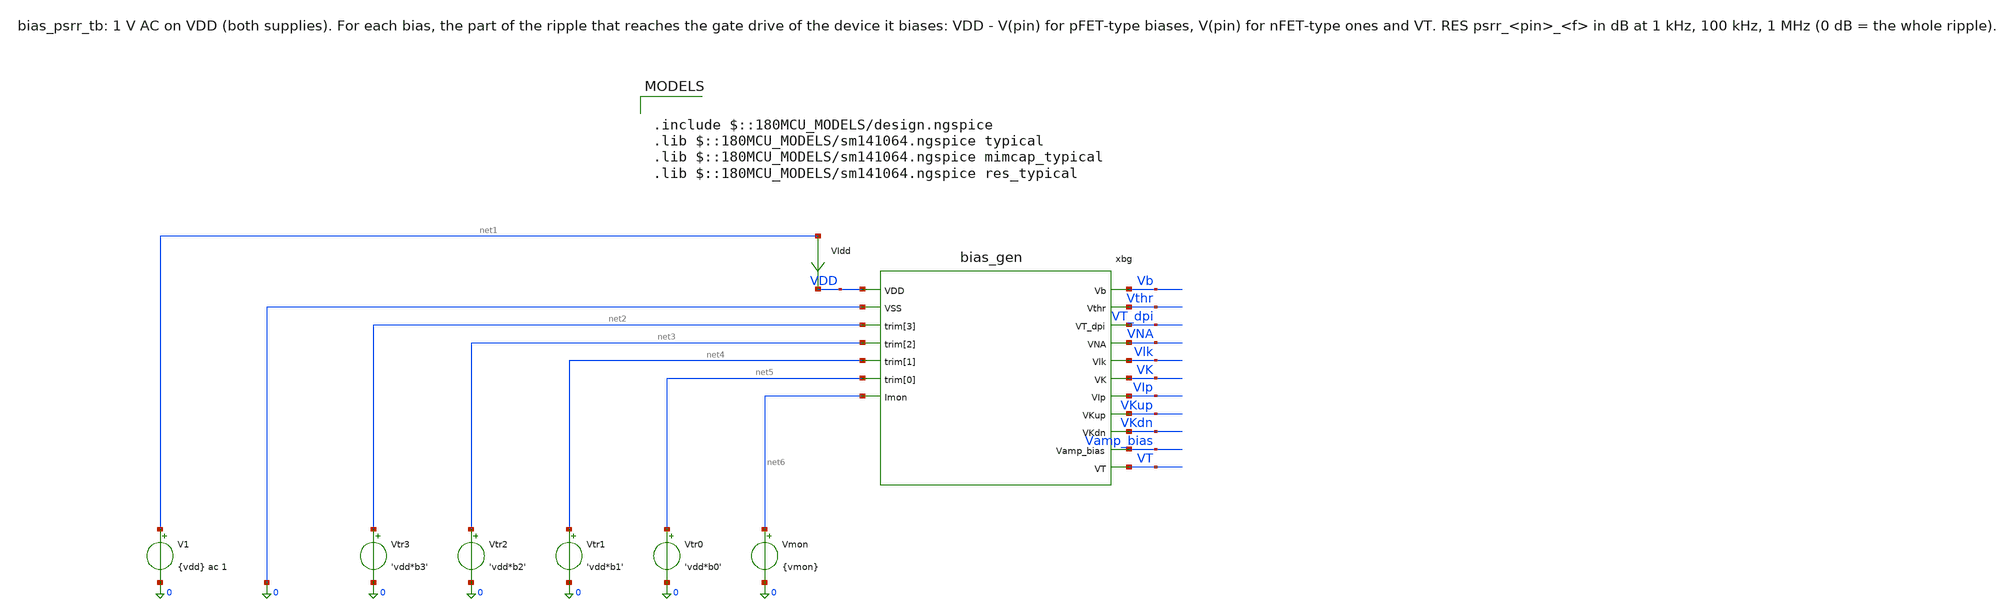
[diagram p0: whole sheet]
** sch_path: analog/bias/testbenches/bias_psrr_tb.sch
**.subckt bias_psrr_tb
xbg VDD 0 net2 net3 net4 net5 net6 Vb Vthr VT_dpi VNA Vlk VK VIp VKup VKdn Vamp_bias VT bias_gen
V1 net1 0 {vdd} ac 1
VIdd net1 VDD 0
.save i(vidd)
Vtr3 net2 0 'vdd*b3'
Vtr2 net3 0 'vdd*b2'
Vtr1 net4 0 'vdd*b1'
Vtr0 net5 0 'vdd*b0'
Vmon net6 0 {vmon}
**** begin user architecture code

.include $::180MCU_MODELS/design.ngspice
.lib $::180MCU_MODELS/sm141064.ngspice typical
.lib $::180MCU_MODELS/sm141064.ngspice mimcap_typical
.lib $::180MCU_MODELS/sm141064.ngspice res_typical



.param vdd=3.3 code=9 vmon=1.65
* trim bits of 'code' (b3 = MSB), driven by Vtr3..Vtr0
.param b3='floor(code/8)-2*floor(code/16)' b2='floor(code/4)-2*floor(code/8)'
.param b1='floor(code/2)-2*floor(code/4)' b0='code-2*floor(code/2)'
.csparam code_c={code}
.csparam vdd_c={vdd}
.control
  save all
  ac dec 10 1 100meg
  let ps_Vb = db(v(Vb))
  meas ac psrr_Vb_1k find ps_Vb at=1k
  echo RES psrr_Vb_1k=$&psrr_Vb_1k
  meas ac psrr_Vb_100k find ps_Vb at=100k
  echo RES psrr_Vb_100k=$&psrr_Vb_100k
  meas ac psrr_Vb_1M find ps_Vb at=1meg
  echo RES psrr_Vb_1M=$&psrr_Vb_1M
  let ps_Vthr = db(1 - v(Vthr))
  meas ac psrr_Vthr_1k find ps_Vthr at=1k
  echo RES psrr_Vthr_1k=$&psrr_Vthr_1k
  meas ac psrr_Vthr_100k find ps_Vthr at=100k
  echo RES psrr_Vthr_100k=$&psrr_Vthr_100k
  meas ac psrr_Vthr_1M find ps_Vthr at=1meg
  echo RES psrr_Vthr_1M=$&psrr_Vthr_1M
  let ps_VT_dpi = db(1 - v(VT_dpi))
  meas ac psrr_VT_dpi_1k find ps_VT_dpi at=1k
  echo RES psrr_VT_dpi_1k=$&psrr_VT_dpi_1k
  meas ac psrr_VT_dpi_100k find ps_VT_dpi at=100k
  echo RES psrr_VT_dpi_100k=$&psrr_VT_dpi_100k
  meas ac psrr_VT_dpi_1M find ps_VT_dpi at=1meg
  echo RES psrr_VT_dpi_1M=$&psrr_VT_dpi_1M
  let ps_VNA = db(1 - v(VNA))
  meas ac psrr_VNA_1k find ps_VNA at=1k
  echo RES psrr_VNA_1k=$&psrr_VNA_1k
  meas ac psrr_VNA_100k find ps_VNA at=100k
  echo RES psrr_VNA_100k=$&psrr_VNA_100k
  meas ac psrr_VNA_1M find ps_VNA at=1meg
  echo RES psrr_VNA_1M=$&psrr_VNA_1M
  let ps_Vlk = db(v(Vlk))
  meas ac psrr_Vlk_1k find ps_Vlk at=1k
  echo RES psrr_Vlk_1k=$&psrr_Vlk_1k
  meas ac psrr_Vlk_100k find ps_Vlk at=100k
  echo RES psrr_Vlk_100k=$&psrr_Vlk_100k
  meas ac psrr_Vlk_1M find ps_Vlk at=1meg
  echo RES psrr_Vlk_1M=$&psrr_Vlk_1M
  let ps_VK = db(v(VK))
  meas ac psrr_VK_1k find ps_VK at=1k
  echo RES psrr_VK_1k=$&psrr_VK_1k
  meas ac psrr_VK_100k find ps_VK at=100k
  echo RES psrr_VK_100k=$&psrr_VK_100k
  meas ac psrr_VK_1M find ps_VK at=1meg
  echo RES psrr_VK_1M=$&psrr_VK_1M
  let ps_VIp = db(v(VIp))
  meas ac psrr_VIp_1k find ps_VIp at=1k
  echo RES psrr_VIp_1k=$&psrr_VIp_1k
  meas ac psrr_VIp_100k find ps_VIp at=100k
  echo RES psrr_VIp_100k=$&psrr_VIp_100k
  meas ac psrr_VIp_1M find ps_VIp at=1meg
  echo RES psrr_VIp_1M=$&psrr_VIp_1M
  let ps_VKup = db(1 - v(VKup))
  meas ac psrr_VKup_1k find ps_VKup at=1k
  echo RES psrr_VKup_1k=$&psrr_VKup_1k
  meas ac psrr_VKup_100k find ps_VKup at=100k
  echo RES psrr_VKup_100k=$&psrr_VKup_100k
  meas ac psrr_VKup_1M find ps_VKup at=1meg
  echo RES psrr_VKup_1M=$&psrr_VKup_1M
  let ps_VKdn = db(v(VKdn))
  meas ac psrr_VKdn_1k find ps_VKdn at=1k
  echo RES psrr_VKdn_1k=$&psrr_VKdn_1k
  meas ac psrr_VKdn_100k find ps_VKdn at=100k
  echo RES psrr_VKdn_100k=$&psrr_VKdn_100k
  meas ac psrr_VKdn_1M find ps_VKdn at=1meg
  echo RES psrr_VKdn_1M=$&psrr_VKdn_1M
  let ps_Vamp_bias = db(v(Vamp_bias))
  meas ac psrr_Vamp_bias_1k find ps_Vamp_bias at=1k
  echo RES psrr_Vamp_bias_1k=$&psrr_Vamp_bias_1k
  meas ac psrr_Vamp_bias_100k find ps_Vamp_bias at=100k
  echo RES psrr_Vamp_bias_100k=$&psrr_Vamp_bias_100k
  meas ac psrr_Vamp_bias_1M find ps_Vamp_bias at=1meg
  echo RES psrr_Vamp_bias_1M=$&psrr_Vamp_bias_1M
  let ps_VT = db(v(VT))
  meas ac psrr_VT_1k find ps_VT at=1k
  echo RES psrr_VT_1k=$&psrr_VT_1k
  meas ac psrr_VT_100k find ps_VT at=100k
  echo RES psrr_VT_100k=$&psrr_VT_100k
  meas ac psrr_VT_1M find ps_VT at=1meg
  echo RES psrr_VT_1M=$&psrr_VT_1M
  if $?batchmode = 0
    plot ps_Vthr ps_VT_dpi ps_Vlk ps_VK ps_VNA ps_VT xlog title 'Supply ripple at the gate drive (dB)'
  end
.endc


**** end user architecture code
**.ends

* expanding   symbol:  analog/bias/bias_gen.sym # of pins=18
** sym_path: analog/bias/bias_gen.sym
** sch_path: analog/bias/bias_gen.sch
.subckt bias_gen VDD VSS trim[3] trim[2] trim[1] trim[0] Imon Vb Vthr VT_dpi VNA Vlk VK VIp VKup
+ VKdn Vamp_bias VT
*.iopin VDD
*.iopin VSS
*.ipin trim[3]
*.ipin trim[2]
*.ipin trim[1]
*.ipin trim[0]
*.iopin Imon
*.opin Vb
*.opin Vthr
*.opin VT_dpi
*.opin VNA
*.opin Vlk
*.opin VK
*.opin VIp
*.opin VKup
*.opin VKdn
*.opin Vamp_bias
*.opin VT
XM3 Vgp Vgp VDD VDD pfet_03v3 L=6.0u W=1.0u nf=1 ad='int((nf+1)/2) * W/nf * 0.18u' as='int((nf+2)/2) * W/nf * 0.18u'
+ pd='2*int((nf+1)/2) * (W/nf + 0.18u)' ps='2*int((nf+2)/2) * (W/nf + 0.18u)' nrd='0.18u / W' nrs='0.18u / W'
+ sa=0 sb=0 sd=0 m=4
XM4 Vgn Vgp VDD VDD pfet_03v3 L=6.0u W=1.0u nf=1 ad='int((nf+1)/2) * W/nf * 0.18u' as='int((nf+2)/2) * W/nf * 0.18u'
+ pd='2*int((nf+1)/2) * (W/nf + 0.18u)' ps='2*int((nf+2)/2) * (W/nf + 0.18u)' nrd='0.18u / W' nrs='0.18u / W'
+ sa=0 sb=0 sd=0 m=4
XM2 Vgp Vgn Vr VSS nfet_03v3 L=6.0u W=1.0u nf=1 ad='int((nf+1)/2) * W/nf * 0.18u' as='int((nf+2)/2) * W/nf * 0.18u'
+ pd='2*int((nf+1)/2) * (W/nf + 0.18u)' ps='2*int((nf+2)/2) * (W/nf + 0.18u)' nrd='0.18u / W' nrs='0.18u / W'
+ sa=0 sb=0 sd=0 m=64
XM1 Vgn Vgn VSS VSS nfet_03v3 L=6.0u W=1.0u nf=1 ad='int((nf+1)/2) * W/nf * 0.18u' as='int((nf+2)/2) * W/nf * 0.18u'
+ pd='2*int((nf+1)/2) * (W/nf + 0.18u)' ps='2*int((nf+2)/2) * (W/nf + 0.18u)' nrd='0.18u / W' nrs='0.18u / W'
+ sa=0 sb=0 sd=0 m=8
XR15 t3 Vr VSS nwell r_width=2.0e-6 r_length=367.830e-6 m=1
XRT3 t2 t3 VSS nwell r_width=2.0e-6 r_length=178.750e-6 m=1
XMT3 t3 trim[3] t2 VSS nfet_03v3 L=0.28u W=4.0u nf=1 ad='int((nf+1)/2) * W/nf * 0.18u' as='int((nf+2)/2) * W/nf * 0.18u'
+ pd='2*int((nf+1)/2) * (W/nf + 0.18u)' ps='2*int((nf+2)/2) * (W/nf + 0.18u)' nrd='0.18u / W' nrs='0.18u / W'
+ sa=0 sb=0 sd=0 m=4
XRT2 t1 t2 VSS nwell r_width=2.0e-6 r_length=89.375e-6 m=1
XMT2 t2 trim[2] t1 VSS nfet_03v3 L=0.28u W=4.0u nf=1 ad='int((nf+1)/2) * W/nf * 0.18u' as='int((nf+2)/2) * W/nf * 0.18u'
+ pd='2*int((nf+1)/2) * (W/nf + 0.18u)' ps='2*int((nf+2)/2) * (W/nf + 0.18u)' nrd='0.18u / W' nrs='0.18u / W'
+ sa=0 sb=0 sd=0 m=2
XRT1 t0 t1 VSS nwell r_width=2.0e-6 r_length=44.687e-6 m=1
XMT1 t1 trim[1] t0 VSS nfet_03v3 L=0.28u W=4.0u nf=1 ad='int((nf+1)/2) * W/nf * 0.18u' as='int((nf+2)/2) * W/nf * 0.18u'
+ pd='2*int((nf+1)/2) * (W/nf + 0.18u)' ps='2*int((nf+2)/2) * (W/nf + 0.18u)' nrd='0.18u / W' nrs='0.18u / W'
+ sa=0 sb=0 sd=0 m=1
XRT0 VSS t0 VSS nwell r_width=2.0e-6 r_length=22.344e-6 m=1
XMT0 t0 trim[0] VSS VSS nfet_03v3 L=0.28u W=4.0u nf=1 ad='int((nf+1)/2) * W/nf * 0.18u' as='int((nf+2)/2) * W/nf * 0.18u'
+ pd='2*int((nf+1)/2) * (W/nf + 0.18u)' ps='2*int((nf+2)/2) * (W/nf + 0.18u)' nrd='0.18u / W' nrs='0.18u / W'
+ sa=0 sb=0 sd=0 m=1
XMS1_0 net1 VSS VDD VDD pfet_03v3 L=50u W=0.22u nf=1 ad='int((nf+1)/2) * W/nf * 0.18u' as='int((nf+2)/2) * W/nf * 0.18u'
+ pd='2*int((nf+1)/2) * (W/nf + 0.18u)' ps='2*int((nf+2)/2) * (W/nf + 0.18u)' nrd='0.18u / W' nrs='0.18u / W'
+ sa=0 sb=0 sd=0 m=1
XMS1_1 net2 VSS net1 VDD pfet_03v3 L=50u W=0.22u nf=1 ad='int((nf+1)/2) * W/nf * 0.18u' as='int((nf+2)/2) * W/nf * 0.18u'
+ pd='2*int((nf+1)/2) * (W/nf + 0.18u)' ps='2*int((nf+2)/2) * (W/nf + 0.18u)' nrd='0.18u / W' nrs='0.18u / W'
+ sa=0 sb=0 sd=0 m=1
XMS1_2 net3 VSS net2 VDD pfet_03v3 L=50u W=0.22u nf=1 ad='int((nf+1)/2) * W/nf * 0.18u' as='int((nf+2)/2) * W/nf * 0.18u'
+ pd='2*int((nf+1)/2) * (W/nf + 0.18u)' ps='2*int((nf+2)/2) * (W/nf + 0.18u)' nrd='0.18u / W' nrs='0.18u / W'
+ sa=0 sb=0 sd=0 m=1
XMS1_3 X VSS net3 VDD pfet_03v3 L=50u W=0.22u nf=1 ad='int((nf+1)/2) * W/nf * 0.18u' as='int((nf+2)/2) * W/nf * 0.18u'
+ pd='2*int((nf+1)/2) * (W/nf + 0.18u)' ps='2*int((nf+2)/2) * (W/nf + 0.18u)' nrd='0.18u / W' nrs='0.18u / W'
+ sa=0 sb=0 sd=0 m=1
XMS2 X Vgn VSS VSS nfet_03v3 L=6.0u W=1.0u nf=1 ad='int((nf+1)/2) * W/nf * 0.18u' as='int((nf+2)/2) * W/nf * 0.18u'
+ pd='2*int((nf+1)/2) * (W/nf + 0.18u)' ps='2*int((nf+2)/2) * (W/nf + 0.18u)' nrd='0.18u / W' nrs='0.18u / W'
+ sa=0 sb=0 sd=0 m=16
XMS3 Vgp X VSS VSS nfet_03v3 L=4u W=0.5u nf=1 ad='int((nf+1)/2) * W/nf * 0.18u' as='int((nf+2)/2) * W/nf * 0.18u'
+ pd='2*int((nf+1)/2) * (W/nf + 0.18u)' ps='2*int((nf+2)/2) * (W/nf + 0.18u)' nrd='0.18u / W' nrs='0.18u / W'
+ sa=0 sb=0 sd=0 m=1
XMMON Imon Vgn VSS VSS nfet_03v3 L=6.0u W=1.0u nf=1 ad='int((nf+1)/2) * W/nf * 0.18u' as='int((nf+2)/2) * W/nf * 0.18u'
+ pd='2*int((nf+1)/2) * (W/nf + 0.18u)' ps='2*int((nf+2)/2) * (W/nf + 0.18u)' nrd='0.18u / W' nrs='0.18u / W'
+ sa=0 sb=0 sd=0 m=8
XMOVB_0 net4 Vgp VDD VDD pfet_03v3 L=6.0u W=1.0u nf=1 ad='int((nf+1)/2) * W/nf * 0.18u' as='int((nf+2)/2) * W/nf * 0.18u'
+ pd='2*int((nf+1)/2) * (W/nf + 0.18u)' ps='2*int((nf+2)/2) * (W/nf + 0.18u)' nrd='0.18u / W' nrs='0.18u / W'
+ sa=0 sb=0 sd=0 m=5
XMOVB_1 net5 Vgp net4 VDD pfet_03v3 L=6.0u W=1.0u nf=1 ad='int((nf+1)/2) * W/nf * 0.18u' as='int((nf+2)/2) * W/nf * 0.18u'
+ pd='2*int((nf+1)/2) * (W/nf + 0.18u)' ps='2*int((nf+2)/2) * (W/nf + 0.18u)' nrd='0.18u / W' nrs='0.18u / W'
+ sa=0 sb=0 sd=0 m=5
XMOVB_2 net6 Vgp net5 VDD pfet_03v3 L=6.0u W=1.0u nf=1 ad='int((nf+1)/2) * W/nf * 0.18u' as='int((nf+2)/2) * W/nf * 0.18u'
+ pd='2*int((nf+1)/2) * (W/nf + 0.18u)' ps='2*int((nf+2)/2) * (W/nf + 0.18u)' nrd='0.18u / W' nrs='0.18u / W'
+ sa=0 sb=0 sd=0 m=5
XMOVB_3 net7 Vgp net6 VDD pfet_03v3 L=6.0u W=1.0u nf=1 ad='int((nf+1)/2) * W/nf * 0.18u' as='int((nf+2)/2) * W/nf * 0.18u'
+ pd='2*int((nf+1)/2) * (W/nf + 0.18u)' ps='2*int((nf+2)/2) * (W/nf + 0.18u)' nrd='0.18u / W' nrs='0.18u / W'
+ sa=0 sb=0 sd=0 m=5
XMOVB_4 net8 Vgp net7 VDD pfet_03v3 L=6.0u W=1.0u nf=1 ad='int((nf+1)/2) * W/nf * 0.18u' as='int((nf+2)/2) * W/nf * 0.18u'
+ pd='2*int((nf+1)/2) * (W/nf + 0.18u)' ps='2*int((nf+2)/2) * (W/nf + 0.18u)' nrd='0.18u / W' nrs='0.18u / W'
+ sa=0 sb=0 sd=0 m=5
XMOVB_5 Vb Vgp net8 VDD pfet_03v3 L=6.0u W=1.0u nf=1 ad='int((nf+1)/2) * W/nf * 0.18u' as='int((nf+2)/2) * W/nf * 0.18u'
+ pd='2*int((nf+1)/2) * (W/nf + 0.18u)' ps='2*int((nf+2)/2) * (W/nf + 0.18u)' nrd='0.18u / W' nrs='0.18u / W'
+ sa=0 sb=0 sd=0 m=5
XMRVB Vb Vb VSS VSS nfet_03v3 L=8.0u W=1.0u nf=1 ad='int((nf+1)/2) * W/nf * 0.18u' as='int((nf+2)/2) * W/nf * 0.18u'
+ pd='2*int((nf+1)/2) * (W/nf + 0.18u)' ps='2*int((nf+2)/2) * (W/nf + 0.18u)' nrd='0.18u / W' nrs='0.18u / W'
+ sa=0 sb=0 sd=0 m=3
XMCVB VSS Vb VSS VSS nfet_03v3 L=10.0u W=10.0u nf=1 ad='int((nf+1)/2) * W/nf * 0.18u' as='int((nf+2)/2) * W/nf * 0.18u'
+ pd='2*int((nf+1)/2) * (W/nf + 0.18u)' ps='2*int((nf+2)/2) * (W/nf + 0.18u)' nrd='0.18u / W' nrs='0.18u / W'
+ sa=0 sb=0 sd=0 m=1
XMRVTHR Vthr Vthr VDD VDD pfet_03v3 L=0.28u W=0.22u nf=1 ad='int((nf+1)/2) * W/nf * 0.18u' as='int((nf+2)/2) * W/nf * 0.18u'
+ pd='2*int((nf+1)/2) * (W/nf + 0.18u)' ps='2*int((nf+2)/2) * (W/nf + 0.18u)' nrd='0.18u / W' nrs='0.18u / W'
+ sa=0 sb=0 sd=0 m=32
XMOVTHR_0 Vthr Vgn net9 VSS nfet_03v3 L=6.0u W=1.0u nf=1 ad='int((nf+1)/2) * W/nf * 0.18u' as='int((nf+2)/2) * W/nf * 0.18u'
+ pd='2*int((nf+1)/2) * (W/nf + 0.18u)' ps='2*int((nf+2)/2) * (W/nf + 0.18u)' nrd='0.18u / W' nrs='0.18u / W'
+ sa=0 sb=0 sd=0 m=1
XMOVTHR_1 net9 Vgn net10 VSS nfet_03v3 L=6.0u W=1.0u nf=1 ad='int((nf+1)/2) * W/nf * 0.18u' as='int((nf+2)/2) * W/nf * 0.18u'
+ pd='2*int((nf+1)/2) * (W/nf + 0.18u)' ps='2*int((nf+2)/2) * (W/nf + 0.18u)' nrd='0.18u / W' nrs='0.18u / W'
+ sa=0 sb=0 sd=0 m=1
XMOVTHR_2 net10 Vgn net11 VSS nfet_03v3 L=6.0u W=1.0u nf=1 ad='int((nf+1)/2) * W/nf * 0.18u' as='int((nf+2)/2) * W/nf * 0.18u'
+ pd='2*int((nf+1)/2) * (W/nf + 0.18u)' ps='2*int((nf+2)/2) * (W/nf + 0.18u)' nrd='0.18u / W' nrs='0.18u / W'
+ sa=0 sb=0 sd=0 m=1
XMOVTHR_3 net11 Vgn net12 VSS nfet_03v3 L=6.0u W=1.0u nf=1 ad='int((nf+1)/2) * W/nf * 0.18u' as='int((nf+2)/2) * W/nf * 0.18u'
+ pd='2*int((nf+1)/2) * (W/nf + 0.18u)' ps='2*int((nf+2)/2) * (W/nf + 0.18u)' nrd='0.18u / W' nrs='0.18u / W'
+ sa=0 sb=0 sd=0 m=1
XMOVTHR_4 net12 Vgn net13 VSS nfet_03v3 L=6.0u W=1.0u nf=1 ad='int((nf+1)/2) * W/nf * 0.18u' as='int((nf+2)/2) * W/nf * 0.18u'
+ pd='2*int((nf+1)/2) * (W/nf + 0.18u)' ps='2*int((nf+2)/2) * (W/nf + 0.18u)' nrd='0.18u / W' nrs='0.18u / W'
+ sa=0 sb=0 sd=0 m=1
XMOVTHR_5 net13 Vgn net14 VSS nfet_03v3 L=6.0u W=1.0u nf=1 ad='int((nf+1)/2) * W/nf * 0.18u' as='int((nf+2)/2) * W/nf * 0.18u'
+ pd='2*int((nf+1)/2) * (W/nf + 0.18u)' ps='2*int((nf+2)/2) * (W/nf + 0.18u)' nrd='0.18u / W' nrs='0.18u / W'
+ sa=0 sb=0 sd=0 m=1
XMOVTHR_6 net14 Vgn net15 VSS nfet_03v3 L=6.0u W=1.0u nf=1 ad='int((nf+1)/2) * W/nf * 0.18u' as='int((nf+2)/2) * W/nf * 0.18u'
+ pd='2*int((nf+1)/2) * (W/nf + 0.18u)' ps='2*int((nf+2)/2) * (W/nf + 0.18u)' nrd='0.18u / W' nrs='0.18u / W'
+ sa=0 sb=0 sd=0 m=1
XMOVTHR_7 net15 Vgn net16 VSS nfet_03v3 L=6.0u W=1.0u nf=1 ad='int((nf+1)/2) * W/nf * 0.18u' as='int((nf+2)/2) * W/nf * 0.18u'
+ pd='2*int((nf+1)/2) * (W/nf + 0.18u)' ps='2*int((nf+2)/2) * (W/nf + 0.18u)' nrd='0.18u / W' nrs='0.18u / W'
+ sa=0 sb=0 sd=0 m=1
XMOVTHR_8 net16 Vgn net17 VSS nfet_03v3 L=6.0u W=1.0u nf=1 ad='int((nf+1)/2) * W/nf * 0.18u' as='int((nf+2)/2) * W/nf * 0.18u'
+ pd='2*int((nf+1)/2) * (W/nf + 0.18u)' ps='2*int((nf+2)/2) * (W/nf + 0.18u)' nrd='0.18u / W' nrs='0.18u / W'
+ sa=0 sb=0 sd=0 m=1
XMOVTHR_9 net17 Vgn net18 VSS nfet_03v3 L=6.0u W=1.0u nf=1 ad='int((nf+1)/2) * W/nf * 0.18u' as='int((nf+2)/2) * W/nf * 0.18u'
+ pd='2*int((nf+1)/2) * (W/nf + 0.18u)' ps='2*int((nf+2)/2) * (W/nf + 0.18u)' nrd='0.18u / W' nrs='0.18u / W'
+ sa=0 sb=0 sd=0 m=1
XMOVTHR_10 net18 Vgn net19 VSS nfet_03v3 L=6.0u W=1.0u nf=1 ad='int((nf+1)/2) * W/nf * 0.18u' as='int((nf+2)/2) * W/nf * 0.18u'
+ pd='2*int((nf+1)/2) * (W/nf + 0.18u)' ps='2*int((nf+2)/2) * (W/nf + 0.18u)' nrd='0.18u / W' nrs='0.18u / W'
+ sa=0 sb=0 sd=0 m=1
XMOVTHR_11 net19 Vgn net20 VSS nfet_03v3 L=6.0u W=1.0u nf=1 ad='int((nf+1)/2) * W/nf * 0.18u' as='int((nf+2)/2) * W/nf * 0.18u'
+ pd='2*int((nf+1)/2) * (W/nf + 0.18u)' ps='2*int((nf+2)/2) * (W/nf + 0.18u)' nrd='0.18u / W' nrs='0.18u / W'
+ sa=0 sb=0 sd=0 m=1
XMOVTHR_12 net20 Vgn net21 VSS nfet_03v3 L=6.0u W=1.0u nf=1 ad='int((nf+1)/2) * W/nf * 0.18u' as='int((nf+2)/2) * W/nf * 0.18u'
+ pd='2*int((nf+1)/2) * (W/nf + 0.18u)' ps='2*int((nf+2)/2) * (W/nf + 0.18u)' nrd='0.18u / W' nrs='0.18u / W'
+ sa=0 sb=0 sd=0 m=1
XMOVTHR_13 net21 Vgn net22 VSS nfet_03v3 L=6.0u W=1.0u nf=1 ad='int((nf+1)/2) * W/nf * 0.18u' as='int((nf+2)/2) * W/nf * 0.18u'
+ pd='2*int((nf+1)/2) * (W/nf + 0.18u)' ps='2*int((nf+2)/2) * (W/nf + 0.18u)' nrd='0.18u / W' nrs='0.18u / W'
+ sa=0 sb=0 sd=0 m=1
XMOVTHR_14 net22 Vgn VSS VSS nfet_03v3 L=6.0u W=1.0u nf=1 ad='int((nf+1)/2) * W/nf * 0.18u' as='int((nf+2)/2) * W/nf * 0.18u'
+ pd='2*int((nf+1)/2) * (W/nf + 0.18u)' ps='2*int((nf+2)/2) * (W/nf + 0.18u)' nrd='0.18u / W' nrs='0.18u / W'
+ sa=0 sb=0 sd=0 m=1
XMCVTHR VDD Vthr VDD VDD pfet_03v3 L=10.0u W=10.0u nf=1 ad='int((nf+1)/2) * W/nf * 0.18u' as='int((nf+2)/2) * W/nf * 0.18u'
+ pd='2*int((nf+1)/2) * (W/nf + 0.18u)' ps='2*int((nf+2)/2) * (W/nf + 0.18u)' nrd='0.18u / W' nrs='0.18u / W'
+ sa=0 sb=0 sd=0 m=1
XMRVT_DPI VT_dpi VT_dpi VDD VDD pfet_03v3 L=0.28u W=0.22u nf=1 ad='int((nf+1)/2) * W/nf * 0.18u' as='int((nf+2)/2) * W/nf * 0.18u'
+ pd='2*int((nf+1)/2) * (W/nf + 0.18u)' ps='2*int((nf+2)/2) * (W/nf + 0.18u)' nrd='0.18u / W' nrs='0.18u / W'
+ sa=0 sb=0 sd=0 m=32
XMOVT_DPI_0 VT_dpi Vgn net23 VSS nfet_03v3 L=6.0u W=1.0u nf=1 ad='int((nf+1)/2) * W/nf * 0.18u' as='int((nf+2)/2) * W/nf * 0.18u'
+ pd='2*int((nf+1)/2) * (W/nf + 0.18u)' ps='2*int((nf+2)/2) * (W/nf + 0.18u)' nrd='0.18u / W' nrs='0.18u / W'
+ sa=0 sb=0 sd=0 m=2
XMOVT_DPI_1 net23 Vgn net24 VSS nfet_03v3 L=6.0u W=1.0u nf=1 ad='int((nf+1)/2) * W/nf * 0.18u' as='int((nf+2)/2) * W/nf * 0.18u'
+ pd='2*int((nf+1)/2) * (W/nf + 0.18u)' ps='2*int((nf+2)/2) * (W/nf + 0.18u)' nrd='0.18u / W' nrs='0.18u / W'
+ sa=0 sb=0 sd=0 m=2
XMOVT_DPI_2 net24 Vgn net25 VSS nfet_03v3 L=6.0u W=1.0u nf=1 ad='int((nf+1)/2) * W/nf * 0.18u' as='int((nf+2)/2) * W/nf * 0.18u'
+ pd='2*int((nf+1)/2) * (W/nf + 0.18u)' ps='2*int((nf+2)/2) * (W/nf + 0.18u)' nrd='0.18u / W' nrs='0.18u / W'
+ sa=0 sb=0 sd=0 m=2
XMOVT_DPI_3 net25 Vgn net26 VSS nfet_03v3 L=6.0u W=1.0u nf=1 ad='int((nf+1)/2) * W/nf * 0.18u' as='int((nf+2)/2) * W/nf * 0.18u'
+ pd='2*int((nf+1)/2) * (W/nf + 0.18u)' ps='2*int((nf+2)/2) * (W/nf + 0.18u)' nrd='0.18u / W' nrs='0.18u / W'
+ sa=0 sb=0 sd=0 m=2
XMOVT_DPI_4 net26 Vgn net27 VSS nfet_03v3 L=6.0u W=1.0u nf=1 ad='int((nf+1)/2) * W/nf * 0.18u' as='int((nf+2)/2) * W/nf * 0.18u'
+ pd='2*int((nf+1)/2) * (W/nf + 0.18u)' ps='2*int((nf+2)/2) * (W/nf + 0.18u)' nrd='0.18u / W' nrs='0.18u / W'
+ sa=0 sb=0 sd=0 m=2
XMOVT_DPI_5 net27 Vgn net28 VSS nfet_03v3 L=6.0u W=1.0u nf=1 ad='int((nf+1)/2) * W/nf * 0.18u' as='int((nf+2)/2) * W/nf * 0.18u'
+ pd='2*int((nf+1)/2) * (W/nf + 0.18u)' ps='2*int((nf+2)/2) * (W/nf + 0.18u)' nrd='0.18u / W' nrs='0.18u / W'
+ sa=0 sb=0 sd=0 m=2
XMOVT_DPI_6 net28 Vgn net29 VSS nfet_03v3 L=6.0u W=1.0u nf=1 ad='int((nf+1)/2) * W/nf * 0.18u' as='int((nf+2)/2) * W/nf * 0.18u'
+ pd='2*int((nf+1)/2) * (W/nf + 0.18u)' ps='2*int((nf+2)/2) * (W/nf + 0.18u)' nrd='0.18u / W' nrs='0.18u / W'
+ sa=0 sb=0 sd=0 m=2
XMOVT_DPI_7 net29 Vgn net30 VSS nfet_03v3 L=6.0u W=1.0u nf=1 ad='int((nf+1)/2) * W/nf * 0.18u' as='int((nf+2)/2) * W/nf * 0.18u'
+ pd='2*int((nf+1)/2) * (W/nf + 0.18u)' ps='2*int((nf+2)/2) * (W/nf + 0.18u)' nrd='0.18u / W' nrs='0.18u / W'
+ sa=0 sb=0 sd=0 m=2
XMOVT_DPI_8 net30 Vgn net31 VSS nfet_03v3 L=6.0u W=1.0u nf=1 ad='int((nf+1)/2) * W/nf * 0.18u' as='int((nf+2)/2) * W/nf * 0.18u'
+ pd='2*int((nf+1)/2) * (W/nf + 0.18u)' ps='2*int((nf+2)/2) * (W/nf + 0.18u)' nrd='0.18u / W' nrs='0.18u / W'
+ sa=0 sb=0 sd=0 m=2
XMOVT_DPI_9 net31 Vgn net32 VSS nfet_03v3 L=6.0u W=1.0u nf=1 ad='int((nf+1)/2) * W/nf * 0.18u' as='int((nf+2)/2) * W/nf * 0.18u'
+ pd='2*int((nf+1)/2) * (W/nf + 0.18u)' ps='2*int((nf+2)/2) * (W/nf + 0.18u)' nrd='0.18u / W' nrs='0.18u / W'
+ sa=0 sb=0 sd=0 m=2
XMOVT_DPI_10 net32 Vgn net33 VSS nfet_03v3 L=6.0u W=1.0u nf=1 ad='int((nf+1)/2) * W/nf * 0.18u' as='int((nf+2)/2) * W/nf * 0.18u'
+ pd='2*int((nf+1)/2) * (W/nf + 0.18u)' ps='2*int((nf+2)/2) * (W/nf + 0.18u)' nrd='0.18u / W' nrs='0.18u / W'
+ sa=0 sb=0 sd=0 m=2
XMOVT_DPI_11 net33 Vgn net34 VSS nfet_03v3 L=6.0u W=1.0u nf=1 ad='int((nf+1)/2) * W/nf * 0.18u' as='int((nf+2)/2) * W/nf * 0.18u'
+ pd='2*int((nf+1)/2) * (W/nf + 0.18u)' ps='2*int((nf+2)/2) * (W/nf + 0.18u)' nrd='0.18u / W' nrs='0.18u / W'
+ sa=0 sb=0 sd=0 m=2
XMOVT_DPI_12 net34 Vgn net35 VSS nfet_03v3 L=6.0u W=1.0u nf=1 ad='int((nf+1)/2) * W/nf * 0.18u' as='int((nf+2)/2) * W/nf * 0.18u'
+ pd='2*int((nf+1)/2) * (W/nf + 0.18u)' ps='2*int((nf+2)/2) * (W/nf + 0.18u)' nrd='0.18u / W' nrs='0.18u / W'
+ sa=0 sb=0 sd=0 m=2
XMOVT_DPI_13 net35 Vgn net36 VSS nfet_03v3 L=6.0u W=1.0u nf=1 ad='int((nf+1)/2) * W/nf * 0.18u' as='int((nf+2)/2) * W/nf * 0.18u'
+ pd='2*int((nf+1)/2) * (W/nf + 0.18u)' ps='2*int((nf+2)/2) * (W/nf + 0.18u)' nrd='0.18u / W' nrs='0.18u / W'
+ sa=0 sb=0 sd=0 m=2
XMOVT_DPI_14 net36 Vgn net37 VSS nfet_03v3 L=6.0u W=1.0u nf=1 ad='int((nf+1)/2) * W/nf * 0.18u' as='int((nf+2)/2) * W/nf * 0.18u'
+ pd='2*int((nf+1)/2) * (W/nf + 0.18u)' ps='2*int((nf+2)/2) * (W/nf + 0.18u)' nrd='0.18u / W' nrs='0.18u / W'
+ sa=0 sb=0 sd=0 m=2
XMOVT_DPI_15 net37 Vgn net38 VSS nfet_03v3 L=6.0u W=1.0u nf=1 ad='int((nf+1)/2) * W/nf * 0.18u' as='int((nf+2)/2) * W/nf * 0.18u'
+ pd='2*int((nf+1)/2) * (W/nf + 0.18u)' ps='2*int((nf+2)/2) * (W/nf + 0.18u)' nrd='0.18u / W' nrs='0.18u / W'
+ sa=0 sb=0 sd=0 m=2
XMOVT_DPI_16 net38 Vgn net39 VSS nfet_03v3 L=6.0u W=1.0u nf=1 ad='int((nf+1)/2) * W/nf * 0.18u' as='int((nf+2)/2) * W/nf * 0.18u'
+ pd='2*int((nf+1)/2) * (W/nf + 0.18u)' ps='2*int((nf+2)/2) * (W/nf + 0.18u)' nrd='0.18u / W' nrs='0.18u / W'
+ sa=0 sb=0 sd=0 m=2
XMOVT_DPI_17 net39 Vgn net40 VSS nfet_03v3 L=6.0u W=1.0u nf=1 ad='int((nf+1)/2) * W/nf * 0.18u' as='int((nf+2)/2) * W/nf * 0.18u'
+ pd='2*int((nf+1)/2) * (W/nf + 0.18u)' ps='2*int((nf+2)/2) * (W/nf + 0.18u)' nrd='0.18u / W' nrs='0.18u / W'
+ sa=0 sb=0 sd=0 m=2
XMOVT_DPI_18 net40 Vgn net41 VSS nfet_03v3 L=6.0u W=1.0u nf=1 ad='int((nf+1)/2) * W/nf * 0.18u' as='int((nf+2)/2) * W/nf * 0.18u'
+ pd='2*int((nf+1)/2) * (W/nf + 0.18u)' ps='2*int((nf+2)/2) * (W/nf + 0.18u)' nrd='0.18u / W' nrs='0.18u / W'
+ sa=0 sb=0 sd=0 m=2
XMOVT_DPI_19 net41 Vgn net42 VSS nfet_03v3 L=6.0u W=1.0u nf=1 ad='int((nf+1)/2) * W/nf * 0.18u' as='int((nf+2)/2) * W/nf * 0.18u'
+ pd='2*int((nf+1)/2) * (W/nf + 0.18u)' ps='2*int((nf+2)/2) * (W/nf + 0.18u)' nrd='0.18u / W' nrs='0.18u / W'
+ sa=0 sb=0 sd=0 m=2
XMOVT_DPI_20 net42 Vgn net43 VSS nfet_03v3 L=6.0u W=1.0u nf=1 ad='int((nf+1)/2) * W/nf * 0.18u' as='int((nf+2)/2) * W/nf * 0.18u'
+ pd='2*int((nf+1)/2) * (W/nf + 0.18u)' ps='2*int((nf+2)/2) * (W/nf + 0.18u)' nrd='0.18u / W' nrs='0.18u / W'
+ sa=0 sb=0 sd=0 m=2
XMOVT_DPI_21 net43 Vgn net44 VSS nfet_03v3 L=6.0u W=1.0u nf=1 ad='int((nf+1)/2) * W/nf * 0.18u' as='int((nf+2)/2) * W/nf * 0.18u'
+ pd='2*int((nf+1)/2) * (W/nf + 0.18u)' ps='2*int((nf+2)/2) * (W/nf + 0.18u)' nrd='0.18u / W' nrs='0.18u / W'
+ sa=0 sb=0 sd=0 m=2
XMOVT_DPI_22 net44 Vgn VSS VSS nfet_03v3 L=6.0u W=1.0u nf=1 ad='int((nf+1)/2) * W/nf * 0.18u' as='int((nf+2)/2) * W/nf * 0.18u'
+ pd='2*int((nf+1)/2) * (W/nf + 0.18u)' ps='2*int((nf+2)/2) * (W/nf + 0.18u)' nrd='0.18u / W' nrs='0.18u / W'
+ sa=0 sb=0 sd=0 m=2
XMCVT_DPI VDD VT_dpi VDD VDD pfet_03v3 L=10.0u W=10.0u nf=1 ad='int((nf+1)/2) * W/nf * 0.18u' as='int((nf+2)/2) * W/nf * 0.18u'
+ pd='2*int((nf+1)/2) * (W/nf + 0.18u)' ps='2*int((nf+2)/2) * (W/nf + 0.18u)' nrd='0.18u / W' nrs='0.18u / W'
+ sa=0 sb=0 sd=0 m=1
XMRVNA_0 net45 VNA VDD VDD pfet_03v3 L=1.0u W=1.0u nf=1 ad='int((nf+1)/2) * W/nf * 0.18u' as='int((nf+2)/2) * W/nf * 0.18u'
+ pd='2*int((nf+1)/2) * (W/nf + 0.18u)' ps='2*int((nf+2)/2) * (W/nf + 0.18u)' nrd='0.18u / W' nrs='0.18u / W'
+ sa=0 sb=0 sd=0 m=1
XMRVNA_1 net46 VNA net45 VDD pfet_03v3 L=1.0u W=1.0u nf=1 ad='int((nf+1)/2) * W/nf * 0.18u' as='int((nf+2)/2) * W/nf * 0.18u'
+ pd='2*int((nf+1)/2) * (W/nf + 0.18u)' ps='2*int((nf+2)/2) * (W/nf + 0.18u)' nrd='0.18u / W' nrs='0.18u / W'
+ sa=0 sb=0 sd=0 m=1
XMRVNA_2 net47 VNA net46 VDD pfet_03v3 L=1.0u W=1.0u nf=1 ad='int((nf+1)/2) * W/nf * 0.18u' as='int((nf+2)/2) * W/nf * 0.18u'
+ pd='2*int((nf+1)/2) * (W/nf + 0.18u)' ps='2*int((nf+2)/2) * (W/nf + 0.18u)' nrd='0.18u / W' nrs='0.18u / W'
+ sa=0 sb=0 sd=0 m=1
XMRVNA_3 net48 VNA net47 VDD pfet_03v3 L=1.0u W=1.0u nf=1 ad='int((nf+1)/2) * W/nf * 0.18u' as='int((nf+2)/2) * W/nf * 0.18u'
+ pd='2*int((nf+1)/2) * (W/nf + 0.18u)' ps='2*int((nf+2)/2) * (W/nf + 0.18u)' nrd='0.18u / W' nrs='0.18u / W'
+ sa=0 sb=0 sd=0 m=1
XMRVNA_4 net49 VNA net48 VDD pfet_03v3 L=1.0u W=1.0u nf=1 ad='int((nf+1)/2) * W/nf * 0.18u' as='int((nf+2)/2) * W/nf * 0.18u'
+ pd='2*int((nf+1)/2) * (W/nf + 0.18u)' ps='2*int((nf+2)/2) * (W/nf + 0.18u)' nrd='0.18u / W' nrs='0.18u / W'
+ sa=0 sb=0 sd=0 m=1
XMRVNA_5 net50 VNA net49 VDD pfet_03v3 L=1.0u W=1.0u nf=1 ad='int((nf+1)/2) * W/nf * 0.18u' as='int((nf+2)/2) * W/nf * 0.18u'
+ pd='2*int((nf+1)/2) * (W/nf + 0.18u)' ps='2*int((nf+2)/2) * (W/nf + 0.18u)' nrd='0.18u / W' nrs='0.18u / W'
+ sa=0 sb=0 sd=0 m=1
XMRVNA_6 net51 VNA net50 VDD pfet_03v3 L=1.0u W=1.0u nf=1 ad='int((nf+1)/2) * W/nf * 0.18u' as='int((nf+2)/2) * W/nf * 0.18u'
+ pd='2*int((nf+1)/2) * (W/nf + 0.18u)' ps='2*int((nf+2)/2) * (W/nf + 0.18u)' nrd='0.18u / W' nrs='0.18u / W'
+ sa=0 sb=0 sd=0 m=1
XMRVNA_7 net52 VNA net51 VDD pfet_03v3 L=1.0u W=1.0u nf=1 ad='int((nf+1)/2) * W/nf * 0.18u' as='int((nf+2)/2) * W/nf * 0.18u'
+ pd='2*int((nf+1)/2) * (W/nf + 0.18u)' ps='2*int((nf+2)/2) * (W/nf + 0.18u)' nrd='0.18u / W' nrs='0.18u / W'
+ sa=0 sb=0 sd=0 m=1
XMRVNA_8 net53 VNA net52 VDD pfet_03v3 L=1.0u W=1.0u nf=1 ad='int((nf+1)/2) * W/nf * 0.18u' as='int((nf+2)/2) * W/nf * 0.18u'
+ pd='2*int((nf+1)/2) * (W/nf + 0.18u)' ps='2*int((nf+2)/2) * (W/nf + 0.18u)' nrd='0.18u / W' nrs='0.18u / W'
+ sa=0 sb=0 sd=0 m=1
XMRVNA_9 net54 VNA net53 VDD pfet_03v3 L=1.0u W=1.0u nf=1 ad='int((nf+1)/2) * W/nf * 0.18u' as='int((nf+2)/2) * W/nf * 0.18u'
+ pd='2*int((nf+1)/2) * (W/nf + 0.18u)' ps='2*int((nf+2)/2) * (W/nf + 0.18u)' nrd='0.18u / W' nrs='0.18u / W'
+ sa=0 sb=0 sd=0 m=1
XMRVNA_10 net55 VNA net54 VDD pfet_03v3 L=1.0u W=1.0u nf=1 ad='int((nf+1)/2) * W/nf * 0.18u' as='int((nf+2)/2) * W/nf * 0.18u'
+ pd='2*int((nf+1)/2) * (W/nf + 0.18u)' ps='2*int((nf+2)/2) * (W/nf + 0.18u)' nrd='0.18u / W' nrs='0.18u / W'
+ sa=0 sb=0 sd=0 m=1
XMRVNA_11 net56 VNA net55 VDD pfet_03v3 L=1.0u W=1.0u nf=1 ad='int((nf+1)/2) * W/nf * 0.18u' as='int((nf+2)/2) * W/nf * 0.18u'
+ pd='2*int((nf+1)/2) * (W/nf + 0.18u)' ps='2*int((nf+2)/2) * (W/nf + 0.18u)' nrd='0.18u / W' nrs='0.18u / W'
+ sa=0 sb=0 sd=0 m=1
XMRVNA_12 net57 VNA net56 VDD pfet_03v3 L=1.0u W=1.0u nf=1 ad='int((nf+1)/2) * W/nf * 0.18u' as='int((nf+2)/2) * W/nf * 0.18u'
+ pd='2*int((nf+1)/2) * (W/nf + 0.18u)' ps='2*int((nf+2)/2) * (W/nf + 0.18u)' nrd='0.18u / W' nrs='0.18u / W'
+ sa=0 sb=0 sd=0 m=1
XMRVNA_13 net58 VNA net57 VDD pfet_03v3 L=1.0u W=1.0u nf=1 ad='int((nf+1)/2) * W/nf * 0.18u' as='int((nf+2)/2) * W/nf * 0.18u'
+ pd='2*int((nf+1)/2) * (W/nf + 0.18u)' ps='2*int((nf+2)/2) * (W/nf + 0.18u)' nrd='0.18u / W' nrs='0.18u / W'
+ sa=0 sb=0 sd=0 m=1
XMRVNA_14 net59 VNA net58 VDD pfet_03v3 L=1.0u W=1.0u nf=1 ad='int((nf+1)/2) * W/nf * 0.18u' as='int((nf+2)/2) * W/nf * 0.18u'
+ pd='2*int((nf+1)/2) * (W/nf + 0.18u)' ps='2*int((nf+2)/2) * (W/nf + 0.18u)' nrd='0.18u / W' nrs='0.18u / W'
+ sa=0 sb=0 sd=0 m=1
XMRVNA_15 VNA VNA net59 VDD pfet_03v3 L=1.0u W=1.0u nf=1 ad='int((nf+1)/2) * W/nf * 0.18u' as='int((nf+2)/2) * W/nf * 0.18u'
+ pd='2*int((nf+1)/2) * (W/nf + 0.18u)' ps='2*int((nf+2)/2) * (W/nf + 0.18u)' nrd='0.18u / W' nrs='0.18u / W'
+ sa=0 sb=0 sd=0 m=1
XMOVNA_0 VNA Vgn net60 VSS nfet_03v3 L=6.0u W=1.0u nf=1 ad='int((nf+1)/2) * W/nf * 0.18u' as='int((nf+2)/2) * W/nf * 0.18u'
+ pd='2*int((nf+1)/2) * (W/nf + 0.18u)' ps='2*int((nf+2)/2) * (W/nf + 0.18u)' nrd='0.18u / W' nrs='0.18u / W'
+ sa=0 sb=0 sd=0 m=18
XMOVNA_1 net60 Vgn VSS VSS nfet_03v3 L=6.0u W=1.0u nf=1 ad='int((nf+1)/2) * W/nf * 0.18u' as='int((nf+2)/2) * W/nf * 0.18u'
+ pd='2*int((nf+1)/2) * (W/nf + 0.18u)' ps='2*int((nf+2)/2) * (W/nf + 0.18u)' nrd='0.18u / W' nrs='0.18u / W'
+ sa=0 sb=0 sd=0 m=18
XMCVNA VDD VNA VDD VDD pfet_03v3 L=10.0u W=10.0u nf=1 ad='int((nf+1)/2) * W/nf * 0.18u' as='int((nf+2)/2) * W/nf * 0.18u'
+ pd='2*int((nf+1)/2) * (W/nf + 0.18u)' ps='2*int((nf+2)/2) * (W/nf + 0.18u)' nrd='0.18u / W' nrs='0.18u / W'
+ sa=0 sb=0 sd=0 m=1
XMOVLK_0 net61 Vgp VDD VDD pfet_03v3 L=6.0u W=1.0u nf=1 ad='int((nf+1)/2) * W/nf * 0.18u' as='int((nf+2)/2) * W/nf * 0.18u'
+ pd='2*int((nf+1)/2) * (W/nf + 0.18u)' ps='2*int((nf+2)/2) * (W/nf + 0.18u)' nrd='0.18u / W' nrs='0.18u / W'
+ sa=0 sb=0 sd=0 m=1
XMOVLK_1 net62 Vgp net61 VDD pfet_03v3 L=6.0u W=1.0u nf=1 ad='int((nf+1)/2) * W/nf * 0.18u' as='int((nf+2)/2) * W/nf * 0.18u'
+ pd='2*int((nf+1)/2) * (W/nf + 0.18u)' ps='2*int((nf+2)/2) * (W/nf + 0.18u)' nrd='0.18u / W' nrs='0.18u / W'
+ sa=0 sb=0 sd=0 m=1
XMOVLK_2 net63 Vgp net62 VDD pfet_03v3 L=6.0u W=1.0u nf=1 ad='int((nf+1)/2) * W/nf * 0.18u' as='int((nf+2)/2) * W/nf * 0.18u'
+ pd='2*int((nf+1)/2) * (W/nf + 0.18u)' ps='2*int((nf+2)/2) * (W/nf + 0.18u)' nrd='0.18u / W' nrs='0.18u / W'
+ sa=0 sb=0 sd=0 m=1
XMOVLK_3 net64 Vgp net63 VDD pfet_03v3 L=6.0u W=1.0u nf=1 ad='int((nf+1)/2) * W/nf * 0.18u' as='int((nf+2)/2) * W/nf * 0.18u'
+ pd='2*int((nf+1)/2) * (W/nf + 0.18u)' ps='2*int((nf+2)/2) * (W/nf + 0.18u)' nrd='0.18u / W' nrs='0.18u / W'
+ sa=0 sb=0 sd=0 m=1
XMOVLK_4 net65 Vgp net64 VDD pfet_03v3 L=6.0u W=1.0u nf=1 ad='int((nf+1)/2) * W/nf * 0.18u' as='int((nf+2)/2) * W/nf * 0.18u'
+ pd='2*int((nf+1)/2) * (W/nf + 0.18u)' ps='2*int((nf+2)/2) * (W/nf + 0.18u)' nrd='0.18u / W' nrs='0.18u / W'
+ sa=0 sb=0 sd=0 m=1
XMOVLK_5 net66 Vgp net65 VDD pfet_03v3 L=6.0u W=1.0u nf=1 ad='int((nf+1)/2) * W/nf * 0.18u' as='int((nf+2)/2) * W/nf * 0.18u'
+ pd='2*int((nf+1)/2) * (W/nf + 0.18u)' ps='2*int((nf+2)/2) * (W/nf + 0.18u)' nrd='0.18u / W' nrs='0.18u / W'
+ sa=0 sb=0 sd=0 m=1
XMOVLK_6 Vlk Vgp net66 VDD pfet_03v3 L=6.0u W=1.0u nf=1 ad='int((nf+1)/2) * W/nf * 0.18u' as='int((nf+2)/2) * W/nf * 0.18u'
+ pd='2*int((nf+1)/2) * (W/nf + 0.18u)' ps='2*int((nf+2)/2) * (W/nf + 0.18u)' nrd='0.18u / W' nrs='0.18u / W'
+ sa=0 sb=0 sd=0 m=1
XMRVLK Vlk Vlk VSS VSS nfet_03v3 L=1.0u W=1.0u nf=1 ad='int((nf+1)/2) * W/nf * 0.18u' as='int((nf+2)/2) * W/nf * 0.18u'
+ pd='2*int((nf+1)/2) * (W/nf + 0.18u)' ps='2*int((nf+2)/2) * (W/nf + 0.18u)' nrd='0.18u / W' nrs='0.18u / W'
+ sa=0 sb=0 sd=0 m=14
XMCVLK VSS Vlk VSS VSS nfet_03v3 L=10.0u W=10.0u nf=1 ad='int((nf+1)/2) * W/nf * 0.18u' as='int((nf+2)/2) * W/nf * 0.18u'
+ pd='2*int((nf+1)/2) * (W/nf + 0.18u)' ps='2*int((nf+2)/2) * (W/nf + 0.18u)' nrd='0.18u / W' nrs='0.18u / W'
+ sa=0 sb=0 sd=0 m=1
XMOVK VK Vgp VDD VDD pfet_03v3 L=6.0u W=1.0u nf=1 ad='int((nf+1)/2) * W/nf * 0.18u' as='int((nf+2)/2) * W/nf * 0.18u'
+ pd='2*int((nf+1)/2) * (W/nf + 0.18u)' ps='2*int((nf+2)/2) * (W/nf + 0.18u)' nrd='0.18u / W' nrs='0.18u / W'
+ sa=0 sb=0 sd=0 m=17
XMRVK_0 VK VK net67 VSS nfet_03v3 L=1.0u W=1.0u nf=1 ad='int((nf+1)/2) * W/nf * 0.18u' as='int((nf+2)/2) * W/nf * 0.18u'
+ pd='2*int((nf+1)/2) * (W/nf + 0.18u)' ps='2*int((nf+2)/2) * (W/nf + 0.18u)' nrd='0.18u / W' nrs='0.18u / W'
+ sa=0 sb=0 sd=0 m=1
XMRVK_1 net67 VK net68 VSS nfet_03v3 L=1.0u W=1.0u nf=1 ad='int((nf+1)/2) * W/nf * 0.18u' as='int((nf+2)/2) * W/nf * 0.18u'
+ pd='2*int((nf+1)/2) * (W/nf + 0.18u)' ps='2*int((nf+2)/2) * (W/nf + 0.18u)' nrd='0.18u / W' nrs='0.18u / W'
+ sa=0 sb=0 sd=0 m=1
XMRVK_2 net68 VK net69 VSS nfet_03v3 L=1.0u W=1.0u nf=1 ad='int((nf+1)/2) * W/nf * 0.18u' as='int((nf+2)/2) * W/nf * 0.18u'
+ pd='2*int((nf+1)/2) * (W/nf + 0.18u)' ps='2*int((nf+2)/2) * (W/nf + 0.18u)' nrd='0.18u / W' nrs='0.18u / W'
+ sa=0 sb=0 sd=0 m=1
XMRVK_3 net69 VK net70 VSS nfet_03v3 L=1.0u W=1.0u nf=1 ad='int((nf+1)/2) * W/nf * 0.18u' as='int((nf+2)/2) * W/nf * 0.18u'
+ pd='2*int((nf+1)/2) * (W/nf + 0.18u)' ps='2*int((nf+2)/2) * (W/nf + 0.18u)' nrd='0.18u / W' nrs='0.18u / W'
+ sa=0 sb=0 sd=0 m=1
XMRVK_4 net70 VK net71 VSS nfet_03v3 L=1.0u W=1.0u nf=1 ad='int((nf+1)/2) * W/nf * 0.18u' as='int((nf+2)/2) * W/nf * 0.18u'
+ pd='2*int((nf+1)/2) * (W/nf + 0.18u)' ps='2*int((nf+2)/2) * (W/nf + 0.18u)' nrd='0.18u / W' nrs='0.18u / W'
+ sa=0 sb=0 sd=0 m=1
XMRVK_5 net71 VK net72 VSS nfet_03v3 L=1.0u W=1.0u nf=1 ad='int((nf+1)/2) * W/nf * 0.18u' as='int((nf+2)/2) * W/nf * 0.18u'
+ pd='2*int((nf+1)/2) * (W/nf + 0.18u)' ps='2*int((nf+2)/2) * (W/nf + 0.18u)' nrd='0.18u / W' nrs='0.18u / W'
+ sa=0 sb=0 sd=0 m=1
XMRVK_6 net72 VK net73 VSS nfet_03v3 L=1.0u W=1.0u nf=1 ad='int((nf+1)/2) * W/nf * 0.18u' as='int((nf+2)/2) * W/nf * 0.18u'
+ pd='2*int((nf+1)/2) * (W/nf + 0.18u)' ps='2*int((nf+2)/2) * (W/nf + 0.18u)' nrd='0.18u / W' nrs='0.18u / W'
+ sa=0 sb=0 sd=0 m=1
XMRVK_7 net73 VK net74 VSS nfet_03v3 L=1.0u W=1.0u nf=1 ad='int((nf+1)/2) * W/nf * 0.18u' as='int((nf+2)/2) * W/nf * 0.18u'
+ pd='2*int((nf+1)/2) * (W/nf + 0.18u)' ps='2*int((nf+2)/2) * (W/nf + 0.18u)' nrd='0.18u / W' nrs='0.18u / W'
+ sa=0 sb=0 sd=0 m=1
XMRVK_8 net74 VK net75 VSS nfet_03v3 L=1.0u W=1.0u nf=1 ad='int((nf+1)/2) * W/nf * 0.18u' as='int((nf+2)/2) * W/nf * 0.18u'
+ pd='2*int((nf+1)/2) * (W/nf + 0.18u)' ps='2*int((nf+2)/2) * (W/nf + 0.18u)' nrd='0.18u / W' nrs='0.18u / W'
+ sa=0 sb=0 sd=0 m=1
XMRVK_9 net75 VK net76 VSS nfet_03v3 L=1.0u W=1.0u nf=1 ad='int((nf+1)/2) * W/nf * 0.18u' as='int((nf+2)/2) * W/nf * 0.18u'
+ pd='2*int((nf+1)/2) * (W/nf + 0.18u)' ps='2*int((nf+2)/2) * (W/nf + 0.18u)' nrd='0.18u / W' nrs='0.18u / W'
+ sa=0 sb=0 sd=0 m=1
XMRVK_10 net76 VK net77 VSS nfet_03v3 L=1.0u W=1.0u nf=1 ad='int((nf+1)/2) * W/nf * 0.18u' as='int((nf+2)/2) * W/nf * 0.18u'
+ pd='2*int((nf+1)/2) * (W/nf + 0.18u)' ps='2*int((nf+2)/2) * (W/nf + 0.18u)' nrd='0.18u / W' nrs='0.18u / W'
+ sa=0 sb=0 sd=0 m=1
XMRVK_11 net77 VK net78 VSS nfet_03v3 L=1.0u W=1.0u nf=1 ad='int((nf+1)/2) * W/nf * 0.18u' as='int((nf+2)/2) * W/nf * 0.18u'
+ pd='2*int((nf+1)/2) * (W/nf + 0.18u)' ps='2*int((nf+2)/2) * (W/nf + 0.18u)' nrd='0.18u / W' nrs='0.18u / W'
+ sa=0 sb=0 sd=0 m=1
XMRVK_12 net78 VK net79 VSS nfet_03v3 L=1.0u W=1.0u nf=1 ad='int((nf+1)/2) * W/nf * 0.18u' as='int((nf+2)/2) * W/nf * 0.18u'
+ pd='2*int((nf+1)/2) * (W/nf + 0.18u)' ps='2*int((nf+2)/2) * (W/nf + 0.18u)' nrd='0.18u / W' nrs='0.18u / W'
+ sa=0 sb=0 sd=0 m=1
XMRVK_13 net79 VK net80 VSS nfet_03v3 L=1.0u W=1.0u nf=1 ad='int((nf+1)/2) * W/nf * 0.18u' as='int((nf+2)/2) * W/nf * 0.18u'
+ pd='2*int((nf+1)/2) * (W/nf + 0.18u)' ps='2*int((nf+2)/2) * (W/nf + 0.18u)' nrd='0.18u / W' nrs='0.18u / W'
+ sa=0 sb=0 sd=0 m=1
XMRVK_14 net80 VK net81 VSS nfet_03v3 L=1.0u W=1.0u nf=1 ad='int((nf+1)/2) * W/nf * 0.18u' as='int((nf+2)/2) * W/nf * 0.18u'
+ pd='2*int((nf+1)/2) * (W/nf + 0.18u)' ps='2*int((nf+2)/2) * (W/nf + 0.18u)' nrd='0.18u / W' nrs='0.18u / W'
+ sa=0 sb=0 sd=0 m=1
XMRVK_15 net81 VK VSS VSS nfet_03v3 L=1.0u W=1.0u nf=1 ad='int((nf+1)/2) * W/nf * 0.18u' as='int((nf+2)/2) * W/nf * 0.18u'
+ pd='2*int((nf+1)/2) * (W/nf + 0.18u)' ps='2*int((nf+2)/2) * (W/nf + 0.18u)' nrd='0.18u / W' nrs='0.18u / W'
+ sa=0 sb=0 sd=0 m=1
XMCVK VSS VK VSS VSS nfet_03v3 L=10.0u W=10.0u nf=1 ad='int((nf+1)/2) * W/nf * 0.18u' as='int((nf+2)/2) * W/nf * 0.18u'
+ pd='2*int((nf+1)/2) * (W/nf + 0.18u)' ps='2*int((nf+2)/2) * (W/nf + 0.18u)' nrd='0.18u / W' nrs='0.18u / W'
+ sa=0 sb=0 sd=0 m=1
XMOVIP VIp Vgp VDD VDD pfet_03v3 L=6.0u W=1.0u nf=1 ad='int((nf+1)/2) * W/nf * 0.18u' as='int((nf+2)/2) * W/nf * 0.18u'
+ pd='2*int((nf+1)/2) * (W/nf + 0.18u)' ps='2*int((nf+2)/2) * (W/nf + 0.18u)' nrd='0.18u / W' nrs='0.18u / W'
+ sa=0 sb=0 sd=0 m=3
XMRVIP VIp VIp VSS VSS nfet_03v3 L=1.0u W=1.0u nf=1 ad='int((nf+1)/2) * W/nf * 0.18u' as='int((nf+2)/2) * W/nf * 0.18u'
+ pd='2*int((nf+1)/2) * (W/nf + 0.18u)' ps='2*int((nf+2)/2) * (W/nf + 0.18u)' nrd='0.18u / W' nrs='0.18u / W'
+ sa=0 sb=0 sd=0 m=7
XMCVIP VSS VIp VSS VSS nfet_03v3 L=10.0u W=10.0u nf=1 ad='int((nf+1)/2) * W/nf * 0.18u' as='int((nf+2)/2) * W/nf * 0.18u'
+ pd='2*int((nf+1)/2) * (W/nf + 0.18u)' ps='2*int((nf+2)/2) * (W/nf + 0.18u)' nrd='0.18u / W' nrs='0.18u / W'
+ sa=0 sb=0 sd=0 m=1
XMRVKUP_0 net82 VKup VDD VDD pfet_03v3 L=1.0u W=1.0u nf=1 ad='int((nf+1)/2) * W/nf * 0.18u' as='int((nf+2)/2) * W/nf * 0.18u'
+ pd='2*int((nf+1)/2) * (W/nf + 0.18u)' ps='2*int((nf+2)/2) * (W/nf + 0.18u)' nrd='0.18u / W' nrs='0.18u / W'
+ sa=0 sb=0 sd=0 m=1
XMRVKUP_1 VKup VKup net82 VDD pfet_03v3 L=1.0u W=1.0u nf=1 ad='int((nf+1)/2) * W/nf * 0.18u' as='int((nf+2)/2) * W/nf * 0.18u'
+ pd='2*int((nf+1)/2) * (W/nf + 0.18u)' ps='2*int((nf+2)/2) * (W/nf + 0.18u)' nrd='0.18u / W' nrs='0.18u / W'
+ sa=0 sb=0 sd=0 m=1
XMOVKUP_0 VKup Vgn net83 VSS nfet_03v3 L=6.0u W=1.0u nf=1 ad='int((nf+1)/2) * W/nf * 0.18u' as='int((nf+2)/2) * W/nf * 0.18u'
+ pd='2*int((nf+1)/2) * (W/nf + 0.18u)' ps='2*int((nf+2)/2) * (W/nf + 0.18u)' nrd='0.18u / W' nrs='0.18u / W'
+ sa=0 sb=0 sd=0 m=16
XMOVKUP_1 net83 Vgn VSS VSS nfet_03v3 L=6.0u W=1.0u nf=1 ad='int((nf+1)/2) * W/nf * 0.18u' as='int((nf+2)/2) * W/nf * 0.18u'
+ pd='2*int((nf+1)/2) * (W/nf + 0.18u)' ps='2*int((nf+2)/2) * (W/nf + 0.18u)' nrd='0.18u / W' nrs='0.18u / W'
+ sa=0 sb=0 sd=0 m=16
XMCVKUP VDD VKup VDD VDD pfet_03v3 L=10.0u W=10.0u nf=1 ad='int((nf+1)/2) * W/nf * 0.18u' as='int((nf+2)/2) * W/nf * 0.18u'
+ pd='2*int((nf+1)/2) * (W/nf + 0.18u)' ps='2*int((nf+2)/2) * (W/nf + 0.18u)' nrd='0.18u / W' nrs='0.18u / W'
+ sa=0 sb=0 sd=0 m=1
XMOVKDN VKdn Vgp VDD VDD pfet_03v3 L=6.0u W=1.0u nf=1 ad='int((nf+1)/2) * W/nf * 0.18u' as='int((nf+2)/2) * W/nf * 0.18u'
+ pd='2*int((nf+1)/2) * (W/nf + 0.18u)' ps='2*int((nf+2)/2) * (W/nf + 0.18u)' nrd='0.18u / W' nrs='0.18u / W'
+ sa=0 sb=0 sd=0 m=5
XMRVKDN VKdn VKdn VSS VSS nfet_03v3 L=1.0u W=1.0u nf=1 ad='int((nf+1)/2) * W/nf * 0.18u' as='int((nf+2)/2) * W/nf * 0.18u'
+ pd='2*int((nf+1)/2) * (W/nf + 0.18u)' ps='2*int((nf+2)/2) * (W/nf + 0.18u)' nrd='0.18u / W' nrs='0.18u / W'
+ sa=0 sb=0 sd=0 m=8
XMCVKDN VSS VKdn VSS VSS nfet_03v3 L=10.0u W=10.0u nf=1 ad='int((nf+1)/2) * W/nf * 0.18u' as='int((nf+2)/2) * W/nf * 0.18u'
+ pd='2*int((nf+1)/2) * (W/nf + 0.18u)' ps='2*int((nf+2)/2) * (W/nf + 0.18u)' nrd='0.18u / W' nrs='0.18u / W'
+ sa=0 sb=0 sd=0 m=1
XMOVAMP_BIAS Vamp_bias Vgp VDD VDD pfet_03v3 L=6.0u W=1.0u nf=1 ad='int((nf+1)/2) * W/nf * 0.18u' as='int((nf+2)/2) * W/nf * 0.18u'
+ pd='2*int((nf+1)/2) * (W/nf + 0.18u)' ps='2*int((nf+2)/2) * (W/nf + 0.18u)' nrd='0.18u / W' nrs='0.18u / W'
+ sa=0 sb=0 sd=0 m=7
XMRVAMP_BIAS Vamp_bias Vamp_bias VSS VSS nfet_03v3 L=0.28u W=0.22u nf=1 ad='int((nf+1)/2) * W/nf * 0.18u'
+ as='int((nf+2)/2) * W/nf * 0.18u' pd='2*int((nf+1)/2) * (W/nf + 0.18u)' ps='2*int((nf+2)/2) * (W/nf + 0.18u)'
+ nrd='0.18u / W' nrs='0.18u / W' sa=0 sb=0 sd=0 m=4
XMCVAMP_BIAS VSS Vamp_bias VSS VSS nfet_03v3 L=10.0u W=10.0u nf=1 ad='int((nf+1)/2) * W/nf * 0.18u' as='int((nf+2)/2) * W/nf * 0.18u'
+ pd='2*int((nf+1)/2) * (W/nf + 0.18u)' ps='2*int((nf+2)/2) * (W/nf + 0.18u)' nrd='0.18u / W' nrs='0.18u / W'
+ sa=0 sb=0 sd=0 m=1
XMVT0 vt3 vt3 VDD VDD pfet_03v3 L=10.0u W=1.0u nf=1 ad='int((nf+1)/2) * W/nf * 0.18u' as='int((nf+2)/2) * W/nf * 0.18u'
+ pd='2*int((nf+1)/2) * (W/nf + 0.18u)' ps='2*int((nf+2)/2) * (W/nf + 0.18u)' nrd='0.18u / W' nrs='0.18u / W'
+ sa=0 sb=0 sd=0 m=1
XMVT1 VT VT vt3 vt3 pfet_03v3 L=10.0u W=1.0u nf=1 ad='int((nf+1)/2) * W/nf * 0.18u' as='int((nf+2)/2) * W/nf * 0.18u'
+ pd='2*int((nf+1)/2) * (W/nf + 0.18u)' ps='2*int((nf+2)/2) * (W/nf + 0.18u)' nrd='0.18u / W' nrs='0.18u / W'
+ sa=0 sb=0 sd=0 m=1
XMVT2 vt1 vt1 VT VT pfet_03v3 L=10.0u W=1.0u nf=1 ad='int((nf+1)/2) * W/nf * 0.18u' as='int((nf+2)/2) * W/nf * 0.18u'
+ pd='2*int((nf+1)/2) * (W/nf + 0.18u)' ps='2*int((nf+2)/2) * (W/nf + 0.18u)' nrd='0.18u / W' nrs='0.18u / W'
+ sa=0 sb=0 sd=0 m=1
XMVT3 VSS VSS vt1 vt1 pfet_03v3 L=10.0u W=1.0u nf=1 ad='int((nf+1)/2) * W/nf * 0.18u' as='int((nf+2)/2) * W/nf * 0.18u'
+ pd='2*int((nf+1)/2) * (W/nf + 0.18u)' ps='2*int((nf+2)/2) * (W/nf + 0.18u)' nrd='0.18u / W' nrs='0.18u / W'
+ sa=0 sb=0 sd=0 m=1
XMCVT VSS VT VSS VSS nfet_03v3 L=10.0u W=10.0u nf=1 ad='int((nf+1)/2) * W/nf * 0.18u' as='int((nf+2)/2) * W/nf * 0.18u'
+ pd='2*int((nf+1)/2) * (W/nf + 0.18u)' ps='2*int((nf+2)/2) * (W/nf + 0.18u)' nrd='0.18u / W' nrs='0.18u / W'
+ sa=0 sb=0 sd=0 m=1
.ends

.end
